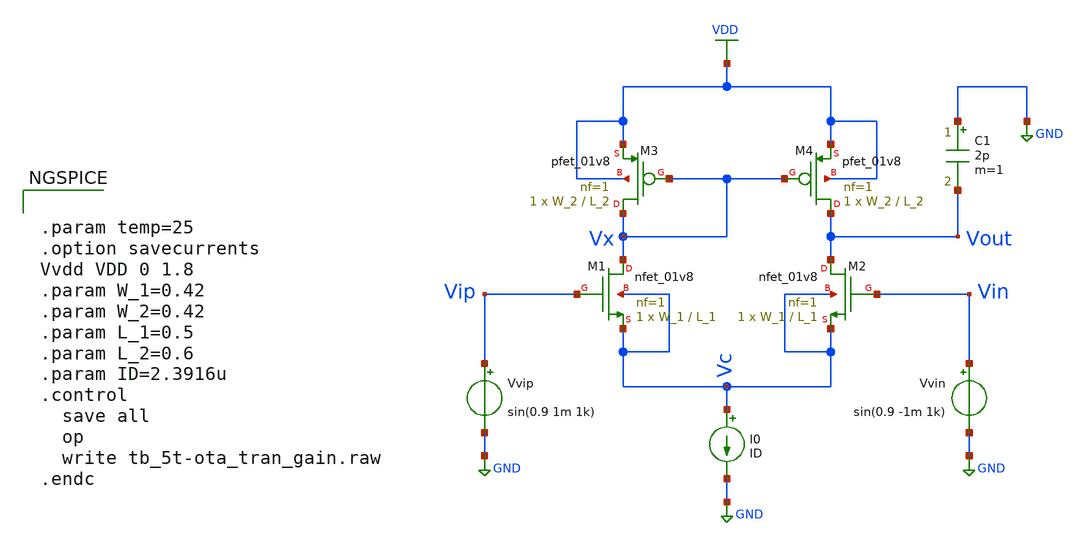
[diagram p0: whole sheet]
** sch_path: Xschem Simulations/5T-OTA/tb_5t-ota_tran_gain.sch
**.subckt tb_5t-ota_tran_gain
XM1 Vx Vip Vc Vc sky130_fd_pr__nfet_01v8 L=L_1 W=W_1 nf=1 ad='int((1 + 1)/2) * W_1 / 1 * 0.29' as='int((1 + 2)/2) * W_1 / 1 * 0.29'
+ pd='2*int((1 + 1)/2) * (W_1 / 1 + 0.29)' ps='2*int((1 + 2)/2) * (W_1 / 1 + 0.29)' nrd='0.29 / W_1 ' nrs='0.29 / W_1 '
+ sa=0 sb=0 sd=0 mult=1 m=1
XM2 Vout Vin Vc Vc sky130_fd_pr__nfet_01v8 L=L_1 W=W_1 nf=1 ad='int((1 + 1)/2) * W_1 / 1 * 0.29' as='int((1 + 2)/2) * W_1 / 1 * 0.29'
+ pd='2*int((1 + 1)/2) * (W_1 / 1 + 0.29)' ps='2*int((1 + 2)/2) * (W_1 / 1 + 0.29)' nrd='0.29 / W_1 ' nrs='0.29 / W_1 '
+ sa=0 sb=0 sd=0 mult=1 m=1
I0 Vc GND ID
Vvip Vip GND sin(0.9 1m 1k)
Vvin Vin GND sin(0.9 -1m 1k)
C1 GND Vout 2p m=1
XM3 Vx Vx VDD VDD sky130_fd_pr__pfet_01v8 L=L_2 W=W_2 nf=1 ad='int((1 + 1)/2) * W_2 / 1 * 0.29' as='int((1 + 2)/2) * W_2 / 1 * 0.29'
+ pd='2*int((1 + 1)/2) * (W_2 / 1 + 0.29)' ps='2*int((1 + 2)/2) * (W_2 / 1 + 0.29)' nrd='0.29 / W_2 ' nrs='0.29 / W_2 '
+ sa=0 sb=0 sd=0 mult=1 m=1
XM4 Vout Vx VDD VDD sky130_fd_pr__pfet_01v8 L=L_2 W=W_2 nf=1 ad='int((1 + 1)/2) * W_2 / 1 * 0.29' as='int((1 + 2)/2) * W_2 / 1 * 0.29'
+ pd='2*int((1 + 1)/2) * (W_2 / 1 + 0.29)' ps='2*int((1 + 2)/2) * (W_2 / 1 + 0.29)' nrd='0.29 / W_2 ' nrs='0.29 / W_2 '
+ sa=0 sb=0 sd=0 mult=1 m=1
**** begin user architecture code

** opencircuitdesign pdks install
.lib $::SKYWATER_MODELS/sky130.lib.spice tt



.param temp=25
.option savecurrents
Vvdd VDD 0 1.8
.param W_1=0.42
.param W_2=0.42
.param L_1=0.5
.param L_2=0.6
.param ID=2.3916u
.control
  save all
  op
  write tb_5t-ota_tran_gain.raw
.endc




.control
  tran 0.1m 2m
  save all

  let v_in = v(vip) - v(vin)
  let v_out = v(vout)

  plot v_in
  plot v_out

  meas tran v_in_pk  PP v_in from=1m to=2m
  meas tran v_out_pk PP v_out from=1m to=2m

  let gain = v_out_pk / v_in_pk
  print gain
  let gain_db = 20 * log10(gain)
  print gain_db
.endc


**** end user architecture code
**.ends
.GLOBAL GND
.GLOBAL VDD
.end
